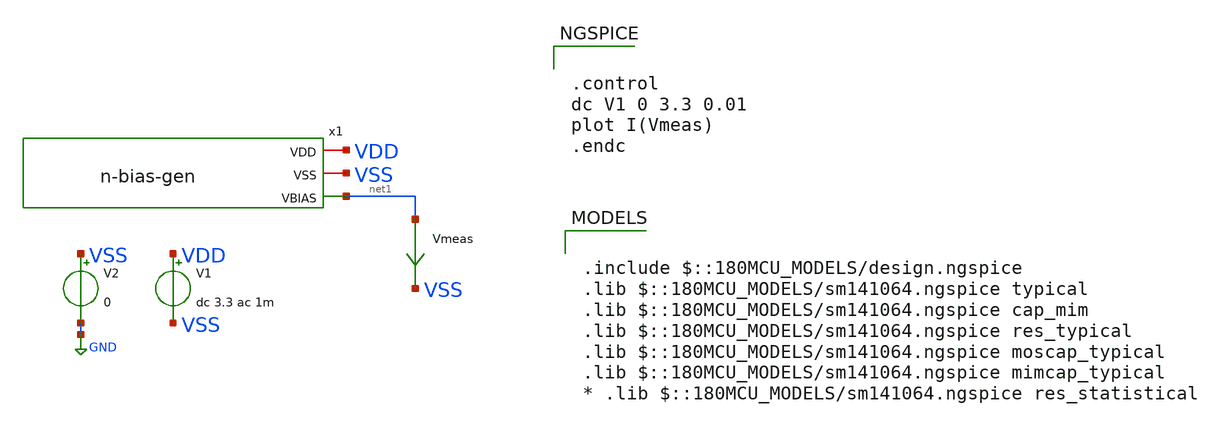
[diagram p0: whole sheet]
** sch_path: w1_advanced-foundation/w1_task/w1_tb/tb_n-bias-gen.sch
**.subckt tb_n-bias-gen
V1 VDD VSS dc 3.3 ac 1m
V2 VSS GND 0
Vmeas net1 VSS 0
.save i(vmeas)
x1 VDD VSS net1 n-bias-gen
**** begin user architecture code

.include $::180MCU_MODELS/design.ngspice
.lib $::180MCU_MODELS/sm141064.ngspice typical
.lib $::180MCU_MODELS/sm141064.ngspice cap_mim
.lib $::180MCU_MODELS/sm141064.ngspice res_typical
.lib $::180MCU_MODELS/sm141064.ngspice moscap_typical
.lib $::180MCU_MODELS/sm141064.ngspice mimcap_typical
* .lib $::180MCU_MODELS/sm141064.ngspice res_statistical



.control
dc V1 0 3.3 0.01
plot I(Vmeas)
.endc


**** end user architecture code
**.ends

* expanding   symbol:
*+  /foss/designs/aic-sems-v/w1_advanced-foundation/w1_task/w1_current_mirror/n-bias-gen.sym # of pins=3
** sym_path: w1_advanced-foundation/w1_task/w1_current_mirror/n-bias-gen.sym
** sch_path: w1_advanced-foundation/w1_task/w1_current_mirror/n-bias-gen.sch
.subckt n-bias-gen VDD VSS VBIAS
*.iopin VDD
*.iopin VSS
*.opin VBIAS
XM1 VBIAS VBIAS VSS VSS nfet_03v3 L=2u W=37.5u nf=1 ad='int((nf+1)/2) * W/nf * 0.18u' as='int((nf+2)/2) * W/nf * 0.18u'
+ pd='2*int((nf+1)/2) * (W/nf + 0.18u)' ps='2*int((nf+2)/2) * (W/nf + 0.18u)' nrd='0.18u / W' nrs='0.18u / W'
+ sa=0 sb=0 sd=0 m=1
XR1 VBIAS net9 VSS ppolyf_u_1k r_width=4e-6 r_length=100e-6 m=1
XR2 net1 VDD VSS ppolyf_u_1k r_width=4e-6 r_length=100e-6 m=1
XR3 net2 net1 VSS ppolyf_u_1k r_width=4e-6 r_length=100e-6 m=1
XR4 net9 net8 VSS ppolyf_u_1k r_width=4e-6 r_length=100e-6 m=1
XR5 net3 net2 VSS ppolyf_u_1k r_width=4e-6 r_length=100e-6 m=1
XR6 net8 net7 VSS ppolyf_u_1k r_width=4e-6 r_length=100e-6 m=1
XR7 net4 net3 VSS ppolyf_u_1k r_width=4e-6 r_length=100e-6 m=1
XR8 net7 net6 VSS ppolyf_u_1k r_width=4e-6 r_length=100e-6 m=1
XR9 net5 net4 VSS ppolyf_u_1k r_width=4e-6 r_length=100e-6 m=1
XR10 net6 net5 VSS ppolyf_u_1k r_width=4e-6 r_length=100e-6 m=1
.ends

.GLOBAL GND
.end
